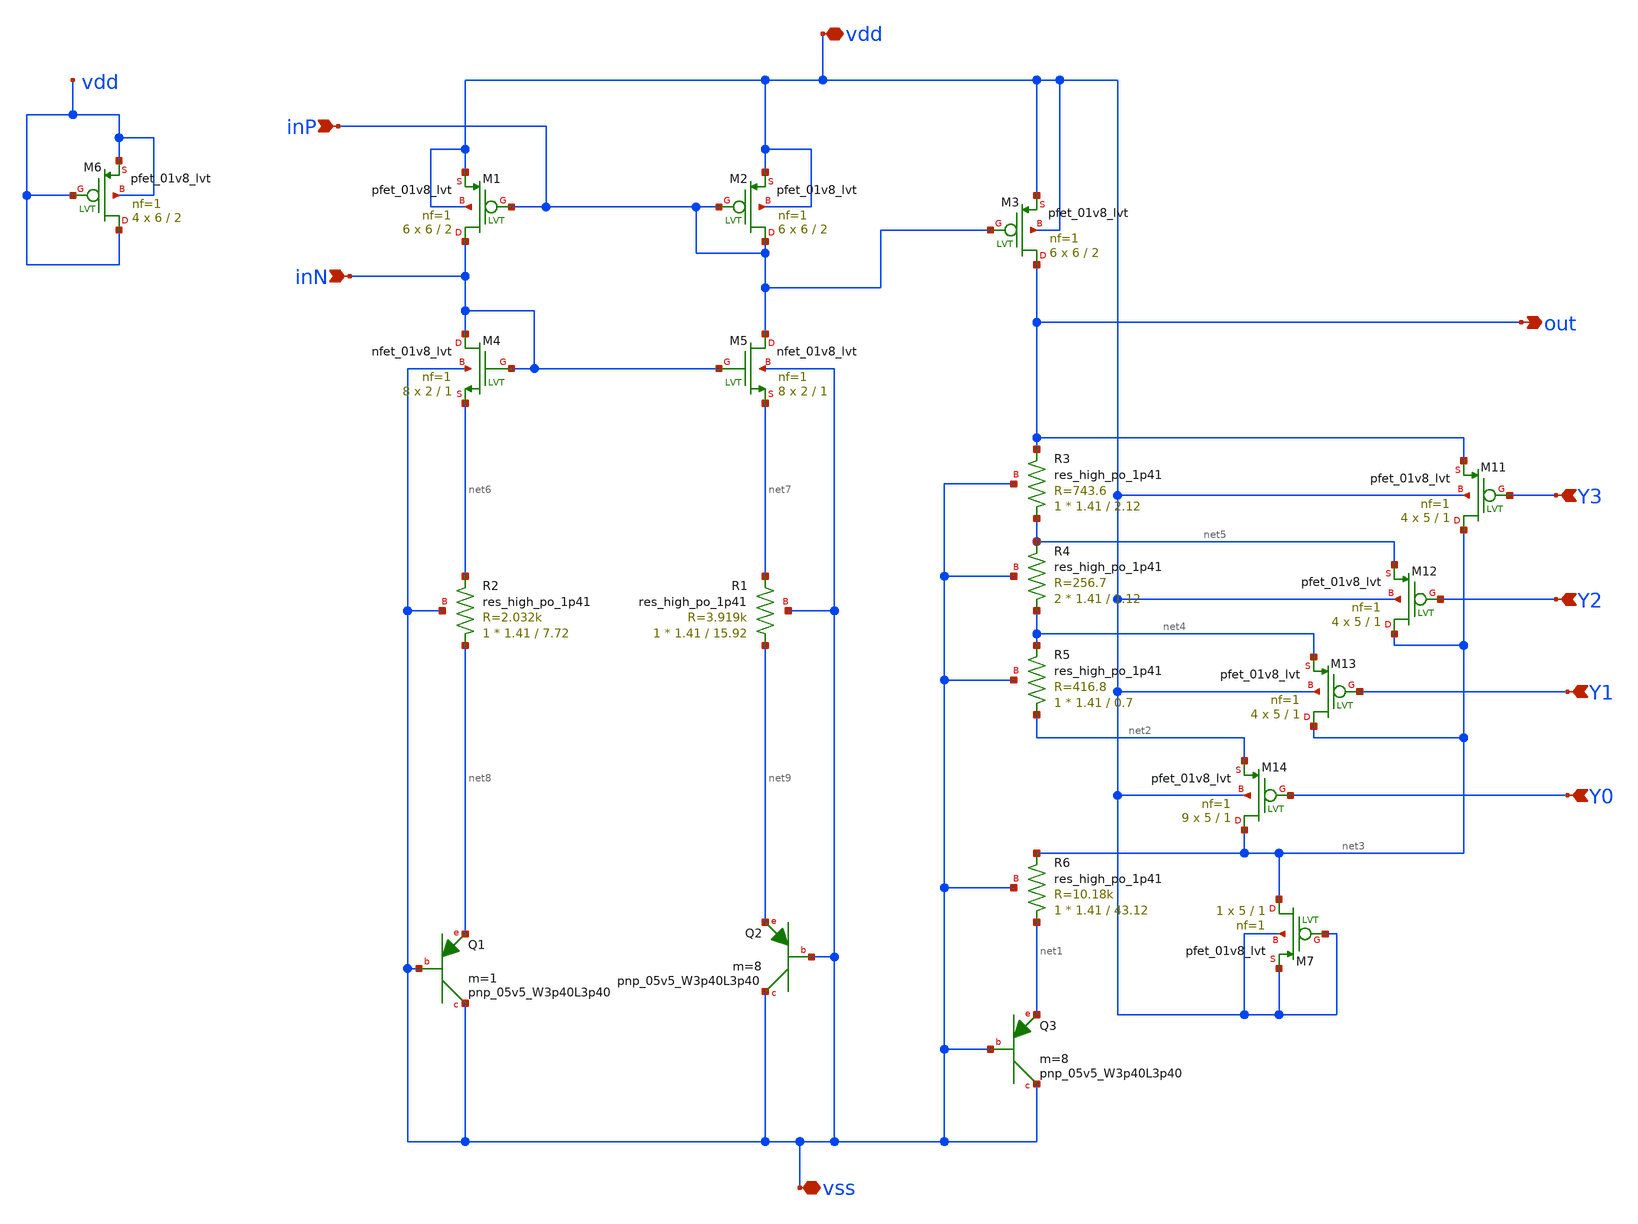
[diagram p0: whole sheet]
** sch_path: BGR_NSL/test/VrefBias.sch
**.subckt VrefBias Y3 Y2 Y1 Y0 vdd vss inP inN out
*.ipin Y3
*.ipin Y2
*.ipin Y1
*.ipin Y0
*.iopin vdd
*.iopin vss
*.ipin inP
*.ipin inN
*.opin out
XM11 net3 Y3 out vdd sky130_fd_pr__pfet_01v8_lvt L=1 W=5 nf=1 ad='int((1 + 1)/2) * 5 / 1 * 0.29' as='int((1 + 2)/2) * 5 / 1 * 0.29'
+ pd='2*int((1 + 1)/2) * (5 / 1 + 0.29)' ps='2*int((1 + 2)/2) * (5 / 1 + 0.29)' nrd='0.29 / 5 ' nrs='0.29 / 5 '
+ sa=0 sb=0 sd=0 mult=4 m=4
XM12 net3 Y2 net5 vdd sky130_fd_pr__pfet_01v8_lvt L=1 W=5 nf=1 ad='int((1 + 1)/2) * 5 / 1 * 0.29' as='int((1 + 2)/2) * 5 / 1 * 0.29'
+ pd='2*int((1 + 1)/2) * (5 / 1 + 0.29)' ps='2*int((1 + 2)/2) * (5 / 1 + 0.29)' nrd='0.29 / 5 ' nrs='0.29 / 5 '
+ sa=0 sb=0 sd=0 mult=4 m=4
XM13 net3 Y1 net4 vdd sky130_fd_pr__pfet_01v8_lvt L=1 W=5 nf=1 ad='int((1 + 1)/2) * 5 / 1 * 0.29' as='int((1 + 2)/2) * 5 / 1 * 0.29'
+ pd='2*int((1 + 1)/2) * (5 / 1 + 0.29)' ps='2*int((1 + 2)/2) * (5 / 1 + 0.29)' nrd='0.29 / 5 ' nrs='0.29 / 5 '
+ sa=0 sb=0 sd=0 mult=4 m=4
XM14 net3 Y0 net2 vdd sky130_fd_pr__pfet_01v8_lvt L=1 W=5 nf=1 ad='int((1 + 1)/2) * 5 / 1 * 0.29' as='int((1 + 2)/2) * 5 / 1 * 0.29'
+ pd='2*int((1 + 1)/2) * (5 / 1 + 0.29)' ps='2*int((1 + 2)/2) * (5 / 1 + 0.29)' nrd='0.29 / 5 ' nrs='0.29 / 5 '
+ sa=0 sb=0 sd=0 mult=9 m=9
XR3 net5 out vss sky130_fd_pr__res_high_po_1p41 L=2.12 mult=1 m=1
XR4 net4 net5 vss sky130_fd_pr__res_high_po_1p41 L=1.12 mult=2 m=2
XR5 net2 net4 vss sky130_fd_pr__res_high_po_1p41 L=0.7 mult=1 m=1
XR6 net1 net3 vss sky130_fd_pr__res_high_po_1p41 L=43.12 mult=1 m=1
XM1 inN inP vdd vdd sky130_fd_pr__pfet_01v8_lvt L=2 W=6 nf=1 ad='int((1 + 1)/2) * 6 / 1 * 0.29' as='int((1 + 2)/2) * 6 / 1 * 0.29'
+ pd='2*int((1 + 1)/2) * (6 / 1 + 0.29)' ps='2*int((1 + 2)/2) * (6 / 1 + 0.29)' nrd='0.29 / 6 ' nrs='0.29 / 6 '
+ sa=0 sb=0 sd=0 mult=6 m=6
XM2 inP inP vdd vdd sky130_fd_pr__pfet_01v8_lvt L=2 W=6 nf=1 ad='int((1 + 1)/2) * 6 / 1 * 0.29' as='int((1 + 2)/2) * 6 / 1 * 0.29'
+ pd='2*int((1 + 1)/2) * (6 / 1 + 0.29)' ps='2*int((1 + 2)/2) * (6 / 1 + 0.29)' nrd='0.29 / 6 ' nrs='0.29 / 6 '
+ sa=0 sb=0 sd=0 mult=6 m=6
XM3 out inP vdd vdd sky130_fd_pr__pfet_01v8_lvt L=2 W=6 nf=1 ad='int((1 + 1)/2) * 6 / 1 * 0.29' as='int((1 + 2)/2) * 6 / 1 * 0.29'
+ pd='2*int((1 + 1)/2) * (6 / 1 + 0.29)' ps='2*int((1 + 2)/2) * (6 / 1 + 0.29)' nrd='0.29 / 6 ' nrs='0.29 / 6 '
+ sa=0 sb=0 sd=0 mult=6 m=6
XM4 inN inN net6 vss sky130_fd_pr__nfet_01v8_lvt L=1 W=2 nf=1 ad='int((1 + 1)/2) * 2 / 1 * 0.29' as='int((1 + 2)/2) * 2 / 1 * 0.29'
+ pd='2*int((1 + 1)/2) * (2 / 1 + 0.29)' ps='2*int((1 + 2)/2) * (2 / 1 + 0.29)' nrd='0.29 / 2 ' nrs='0.29 / 2 '
+ sa=0 sb=0 sd=0 mult=8 m=8
XM5 inP inN net7 vss sky130_fd_pr__nfet_01v8_lvt L=1 W=2 nf=1 ad='int((1 + 1)/2) * 2 / 1 * 0.29' as='int((1 + 2)/2) * 2 / 1 * 0.29'
+ pd='2*int((1 + 1)/2) * (2 / 1 + 0.29)' ps='2*int((1 + 2)/2) * (2 / 1 + 0.29)' nrd='0.29 / 2 ' nrs='0.29 / 2 '
+ sa=0 sb=0 sd=0 mult=8 m=8
XR1 net9 net7 vss sky130_fd_pr__res_high_po_1p41 L=15.92 mult=1 m=1
XR2 net8 net6 vss sky130_fd_pr__res_high_po_1p41 L=7.72 mult=1 m=1
XQ1 vss vss net8 sky130_fd_pr__pnp_05v5_W3p40L3p40 m=1
XQ2 vss vss net9 sky130_fd_pr__pnp_05v5_W3p40L3p40 m=8
XQ3 vss vss net1 sky130_fd_pr__pnp_05v5_W3p40L3p40 m=8
XM6 vdd vdd vdd vdd sky130_fd_pr__pfet_01v8_lvt L=2 W=6 nf=1 ad='int((1 + 1)/2) * 6 / 1 * 0.29' as='int((1 + 2)/2) * 6 / 1 * 0.29'
+ pd='2*int((1 + 1)/2) * (6 / 1 + 0.29)' ps='2*int((1 + 2)/2) * (6 / 1 + 0.29)' nrd='0.29 / 6 ' nrs='0.29 / 6 '
+ sa=0 sb=0 sd=0 mult=4 m=4
XM7 net3 vdd vdd vdd sky130_fd_pr__pfet_01v8_lvt L=1 W=5 nf=1 ad='int((1 + 1)/2) * 5 / 1 * 0.29' as='int((1 + 2)/2) * 5 / 1 * 0.29'
+ pd='2*int((1 + 1)/2) * (5 / 1 + 0.29)' ps='2*int((1 + 2)/2) * (5 / 1 + 0.29)' nrd='0.29 / 5 ' nrs='0.29 / 5 '
+ sa=0 sb=0 sd=0 mult=1 m=1
**.ends
.end
